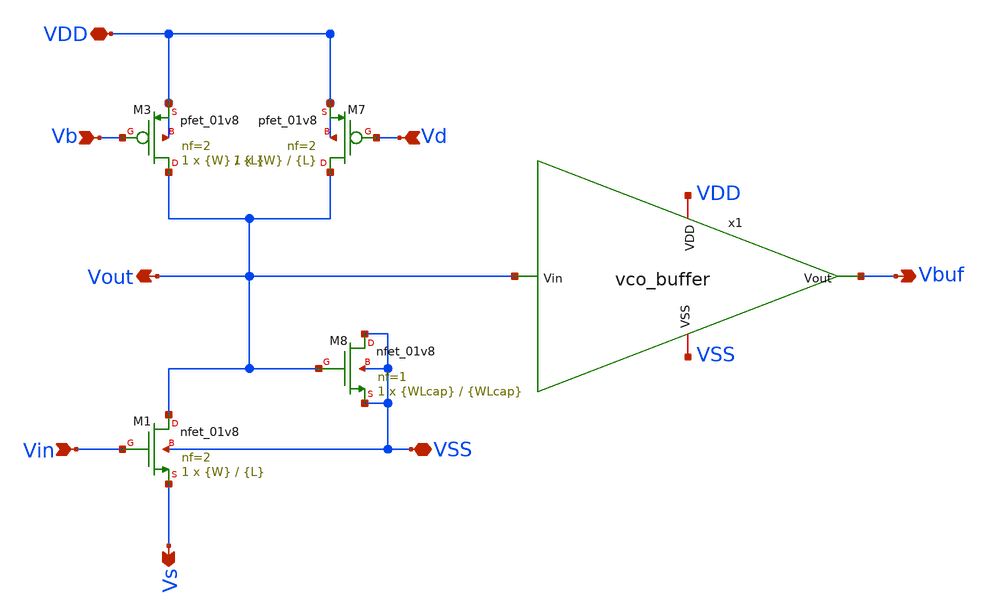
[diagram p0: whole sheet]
** sch_path: xschem/vco_stage_half.sch
**.subckt vco_stage_half VDD VSS Vin Vb Vd Vout Vs Vbuf
*.iopin VDD
*.iopin VSS
*.ipin Vin
*.ipin Vb
*.ipin Vd
*.opin Vout
*.opin Vs
*.opin Vbuf
XM7 Vout Vd VDD VDD sky130_fd_pr__pfet_01v8 L={L} W={W} nf=2 ad='int((nf+1)/2) * W/nf * 0.29' as='int((nf+2)/2) * W/nf * 0.29'
+ pd='2*int((nf+1)/2) * (W/nf + 0.29)' ps='2*int((nf+2)/2) * (W/nf + 0.29)' nrd='0.29 / W' nrs='0.29 / W'
+ sa=0 sb=0 sd=0 mult=1 m=1
XM3 Vout Vb VDD VDD sky130_fd_pr__pfet_01v8 L={L} W={W} nf=2 ad='int((nf+1)/2) * W/nf * 0.29' as='int((nf+2)/2) * W/nf * 0.29'
+ pd='2*int((nf+1)/2) * (W/nf + 0.29)' ps='2*int((nf+2)/2) * (W/nf + 0.29)' nrd='0.29 / W' nrs='0.29 / W'
+ sa=0 sb=0 sd=0 mult=1 m=1
XM1 Vout Vin Vs VSS sky130_fd_pr__nfet_01v8 L={L} W={W} nf=2 ad='int((nf+1)/2) * W/nf * 0.29' as='int((nf+2)/2) * W/nf * 0.29'
+ pd='2*int((nf+1)/2) * (W/nf + 0.29)' ps='2*int((nf+2)/2) * (W/nf + 0.29)' nrd='0.29 / W' nrs='0.29 / W'
+ sa=0 sb=0 sd=0 mult=1 m=1
x1 VDD VSS Vout Vbuf vco_buffer
XM8 VSS Vout VSS VSS sky130_fd_pr__nfet_01v8 L={WLcap} W={WLcap} nf=1 ad='int((nf+1)/2) * W/nf * 0.29'
+ as='int((nf+2)/2) * W/nf * 0.29' pd='2*int((nf+1)/2) * (W/nf + 0.29)' ps='2*int((nf+2)/2) * (W/nf + 0.29)'
+ nrd='0.29 / W' nrs='0.29 / W' sa=0 sb=0 sd=0 mult=1 m=1
**.ends

* expanding   symbol:  vco_buffer.sym # of pins=4
** sym_path: xschem/vco_buffer.sym
** sch_path: xschem/vco_buffer.sch
.subckt vco_buffer VDD VSS Vin Vout
*.iopin VDD
*.iopin VSS
*.ipin Vin
*.opin Vout
x1 VDD Vin net1 VSS vco_inverter
x2 VDD net1 Vout VSS vco_inverter
.ends


* expanding   symbol:  vco_inverter.sym # of pins=4
** sym_path: xschem/vco_inverter.sym
** sch_path: xschem/vco_inverter.sch
.subckt vco_inverter VDD Vin Vout VSS
*.iopin VDD
*.iopin VSS
*.ipin Vin
*.opin Vout
XM1 Vout Vin VSS VSS sky130_fd_pr__nfet_01v8 L=0.15 W=1 nf=1 ad='int((nf+1)/2) * W/nf * 0.29' as='int((nf+2)/2) * W/nf * 0.29'
+ pd='2*int((nf+1)/2) * (W/nf + 0.29)' ps='2*int((nf+2)/2) * (W/nf + 0.29)' nrd='0.29 / W' nrs='0.29 / W'
+ sa=0 sb=0 sd=0 mult=1 m=1
XM2 Vout Vin VDD VDD sky130_fd_pr__pfet_01v8 L=0.15 W=1 nf=1 ad='int((nf+1)/2) * W/nf * 0.29' as='int((nf+2)/2) * W/nf * 0.29'
+ pd='2*int((nf+1)/2) * (W/nf + 0.29)' ps='2*int((nf+2)/2) * (W/nf + 0.29)' nrd='0.29 / W' nrs='0.29 / W'
+ sa=0 sb=0 sd=0 mult=1 m=1
.ends

.end
